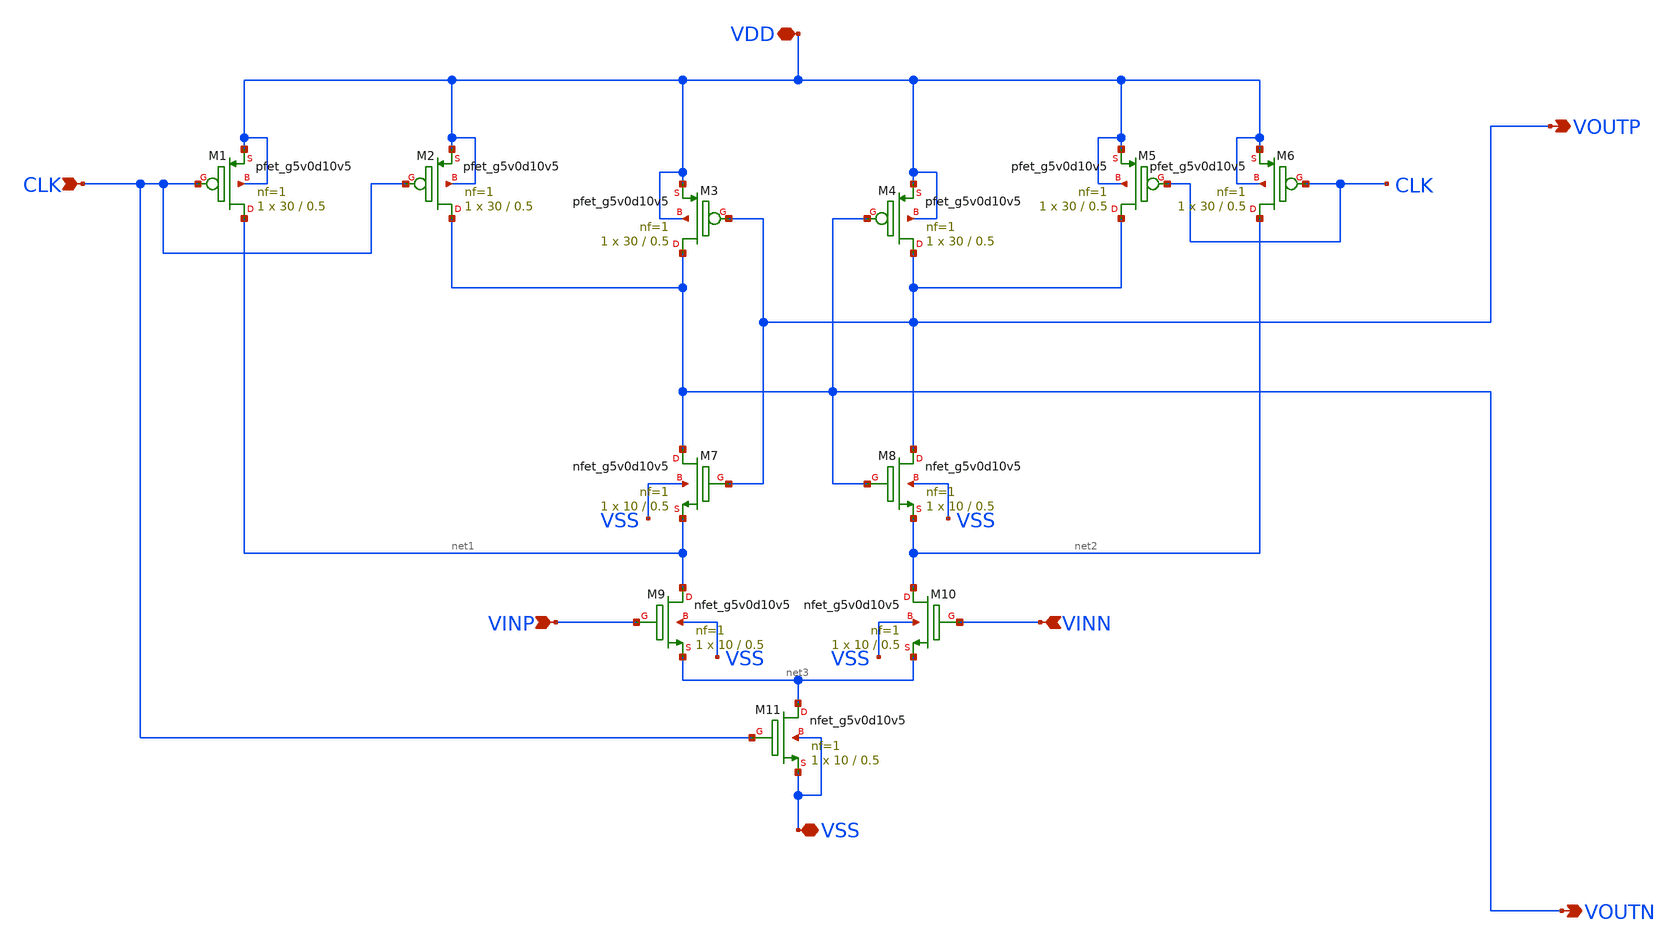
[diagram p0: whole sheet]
** sch_path: xschem/comp_arm.sch
**.subckt comp_arm VSS VDD CLK VINP VINN VOUTN VOUTP
*.iopin VSS
*.iopin VDD
*.ipin CLK
*.ipin VINP
*.ipin VINN
*.opin VOUTN
*.opin VOUTP
XM1 net1 CLK VDD VDD sky130_fd_pr__pfet_g5v0d10v5 L=0.5 W=30 nf=1 ad='int((1 + 1)/2) * 30 / 1 * 0.29'
+ as='int((1 + 2)/2) * 30 / 1 * 0.29' pd='2*int((1 + 1)/2) * (30 / 1 + 0.29)' ps='2*int((1 + 2)/2) * (30 / 1 + 0.29)'
+ nrd='0.29 / 30 ' nrs='0.29 / 30 ' sa=0 sb=0 sd=0 mult=1 m=1
XM2 VOUTN CLK VDD VDD sky130_fd_pr__pfet_g5v0d10v5 L=0.5 W=30 nf=1 ad='int((1 + 1)/2) * 30 / 1 * 0.29'
+ as='int((1 + 2)/2) * 30 / 1 * 0.29' pd='2*int((1 + 1)/2) * (30 / 1 + 0.29)' ps='2*int((1 + 2)/2) * (30 / 1 + 0.29)'
+ nrd='0.29 / 30 ' nrs='0.29 / 30 ' sa=0 sb=0 sd=0 mult=1 m=1
XM3 VOUTN VOUTP VDD VDD sky130_fd_pr__pfet_g5v0d10v5 L=0.5 W=30 nf=1 ad='int((1 + 1)/2) * 30 / 1 * 0.29'
+ as='int((1 + 2)/2) * 30 / 1 * 0.29' pd='2*int((1 + 1)/2) * (30 / 1 + 0.29)' ps='2*int((1 + 2)/2) * (30 / 1 + 0.29)'
+ nrd='0.29 / 30 ' nrs='0.29 / 30 ' sa=0 sb=0 sd=0 mult=1 m=1
XM4 VOUTP VOUTN VDD VDD sky130_fd_pr__pfet_g5v0d10v5 L=0.5 W=30 nf=1 ad='int((1 + 1)/2) * 30 / 1 * 0.29'
+ as='int((1 + 2)/2) * 30 / 1 * 0.29' pd='2*int((1 + 1)/2) * (30 / 1 + 0.29)' ps='2*int((1 + 2)/2) * (30 / 1 + 0.29)'
+ nrd='0.29 / 30 ' nrs='0.29 / 30 ' sa=0 sb=0 sd=0 mult=1 m=1
XM5 VOUTP CLK VDD VDD sky130_fd_pr__pfet_g5v0d10v5 L=0.5 W=30 nf=1 ad='int((1 + 1)/2) * 30 / 1 * 0.29'
+ as='int((1 + 2)/2) * 30 / 1 * 0.29' pd='2*int((1 + 1)/2) * (30 / 1 + 0.29)' ps='2*int((1 + 2)/2) * (30 / 1 + 0.29)'
+ nrd='0.29 / 30 ' nrs='0.29 / 30 ' sa=0 sb=0 sd=0 mult=1 m=1
XM6 net2 CLK VDD VDD sky130_fd_pr__pfet_g5v0d10v5 L=0.5 W=30 nf=1 ad='int((1 + 1)/2) * 30 / 1 * 0.29'
+ as='int((1 + 2)/2) * 30 / 1 * 0.29' pd='2*int((1 + 1)/2) * (30 / 1 + 0.29)' ps='2*int((1 + 2)/2) * (30 / 1 + 0.29)'
+ nrd='0.29 / 30 ' nrs='0.29 / 30 ' sa=0 sb=0 sd=0 mult=1 m=1
XM7 VOUTN VOUTP net1 VSS sky130_fd_pr__nfet_g5v0d10v5 L=0.5 W=10 nf=1 ad='int((1 + 1)/2) * 10 / 1 * 0.29'
+ as='int((1 + 2)/2) * 10 / 1 * 0.29' pd='2*int((1 + 1)/2) * (10 / 1 + 0.29)' ps='2*int((1 + 2)/2) * (10 / 1 + 0.29)'
+ nrd='0.29 / 10 ' nrs='0.29 / 10 ' sa=0 sb=0 sd=0 mult=1 m=1
XM8 VOUTP VOUTN net2 VSS sky130_fd_pr__nfet_g5v0d10v5 L=0.5 W=10 nf=1 ad='int((1 + 1)/2) * 10 / 1 * 0.29'
+ as='int((1 + 2)/2) * 10 / 1 * 0.29' pd='2*int((1 + 1)/2) * (10 / 1 + 0.29)' ps='2*int((1 + 2)/2) * (10 / 1 + 0.29)'
+ nrd='0.29 / 10 ' nrs='0.29 / 10 ' sa=0 sb=0 sd=0 mult=1 m=1
XM9 net1 VINP net3 VSS sky130_fd_pr__nfet_g5v0d10v5 L=0.5 W=10 nf=1 ad='int((1 + 1)/2) * 10 / 1 * 0.29'
+ as='int((1 + 2)/2) * 10 / 1 * 0.29' pd='2*int((1 + 1)/2) * (10 / 1 + 0.29)' ps='2*int((1 + 2)/2) * (10 / 1 + 0.29)'
+ nrd='0.29 / 10 ' nrs='0.29 / 10 ' sa=0 sb=0 sd=0 mult=1 m=1
XM10 net2 VINN net3 VSS sky130_fd_pr__nfet_g5v0d10v5 L=0.5 W=10 nf=1 ad='int((1 + 1)/2) * 10 / 1 * 0.29'
+ as='int((1 + 2)/2) * 10 / 1 * 0.29' pd='2*int((1 + 1)/2) * (10 / 1 + 0.29)' ps='2*int((1 + 2)/2) * (10 / 1 + 0.29)'
+ nrd='0.29 / 10 ' nrs='0.29 / 10 ' sa=0 sb=0 sd=0 mult=1 m=1
XM11 net3 CLK VSS VSS sky130_fd_pr__nfet_g5v0d10v5 L=0.5 W=10 nf=1 ad='int((1 + 1)/2) * 10 / 1 * 0.29'
+ as='int((1 + 2)/2) * 10 / 1 * 0.29' pd='2*int((1 + 1)/2) * (10 / 1 + 0.29)' ps='2*int((1 + 2)/2) * (10 / 1 + 0.29)'
+ nrd='0.29 / 10 ' nrs='0.29 / 10 ' sa=0 sb=0 sd=0 mult=1 m=1
**.ends
.end
